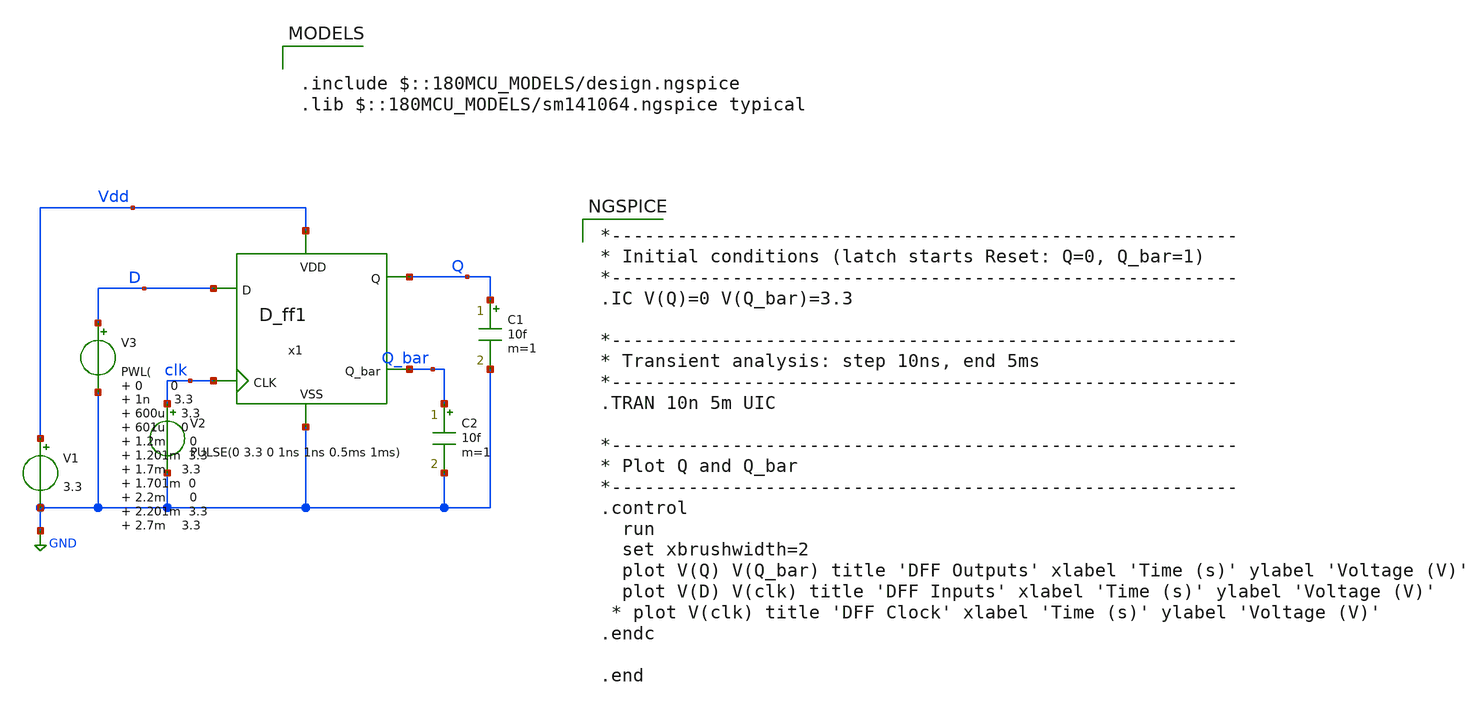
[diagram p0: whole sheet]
** sch_path: designs/libs/core_digital/tb/TB_D_ff1.sch
**.subckt TB_D_ff1
V1 Vdd GND 3.3
C1 Q GND 10f m=1
C2 Q_bar GND 10f m=1
V2 clk GND PULSE(0 3.3 0 1ns 1ns 0.5ms 1ms)
V3 D GND PWL( 0 0 1n 3.3 600u 3.3 601u 0 1.2m 0 1.201m 3.3 1.7m 3.3 1.701m 0 2.2m 0 2.201m 3.3 2.7m
+ 3.3 2.701m 3.3 3.2m 3.3 3.201m 0 3.7m 0 3.701m 3.3 4.2m 3.3 4.201m 0 4.7m 0 4.701m 0 5.2m 0 5.201m 3.3
+ 5.7m 3.3 5.701m 0 6.2m 0
)
x1 Vdd D Q Q_bar clk GND D_ff1
**** begin user architecture code

*---------------------------------------------------------
* Initial conditions (latch starts Reset: Q=0, Q_bar=1)
*---------------------------------------------------------
.IC V(Q)=0 V(Q_bar)=3.3

*---------------------------------------------------------
* Transient analysis: step 10ns, end 5ms
*---------------------------------------------------------
.TRAN 10n 5m UIC

*---------------------------------------------------------
* Plot Q and Q_bar
*---------------------------------------------------------
.control
  run
  set xbrushwidth=2
  plot V(Q) V(Q_bar) title 'DFF Outputs' xlabel 'Time (s)' ylabel 'Voltage (V)'
  plot V(D) V(clk) title 'DFF Inputs' xlabel 'Time (s)' ylabel 'Voltage (V)'
 * plot V(clk) title 'DFF Clock' xlabel 'Time (s)' ylabel 'Voltage (V)'
.endc

.end


.include $::180MCU_MODELS/design.ngspice
.lib $::180MCU_MODELS/sm141064.ngspice typical

**** end user architecture code
**.ends
.GLOBAL GND
.end
